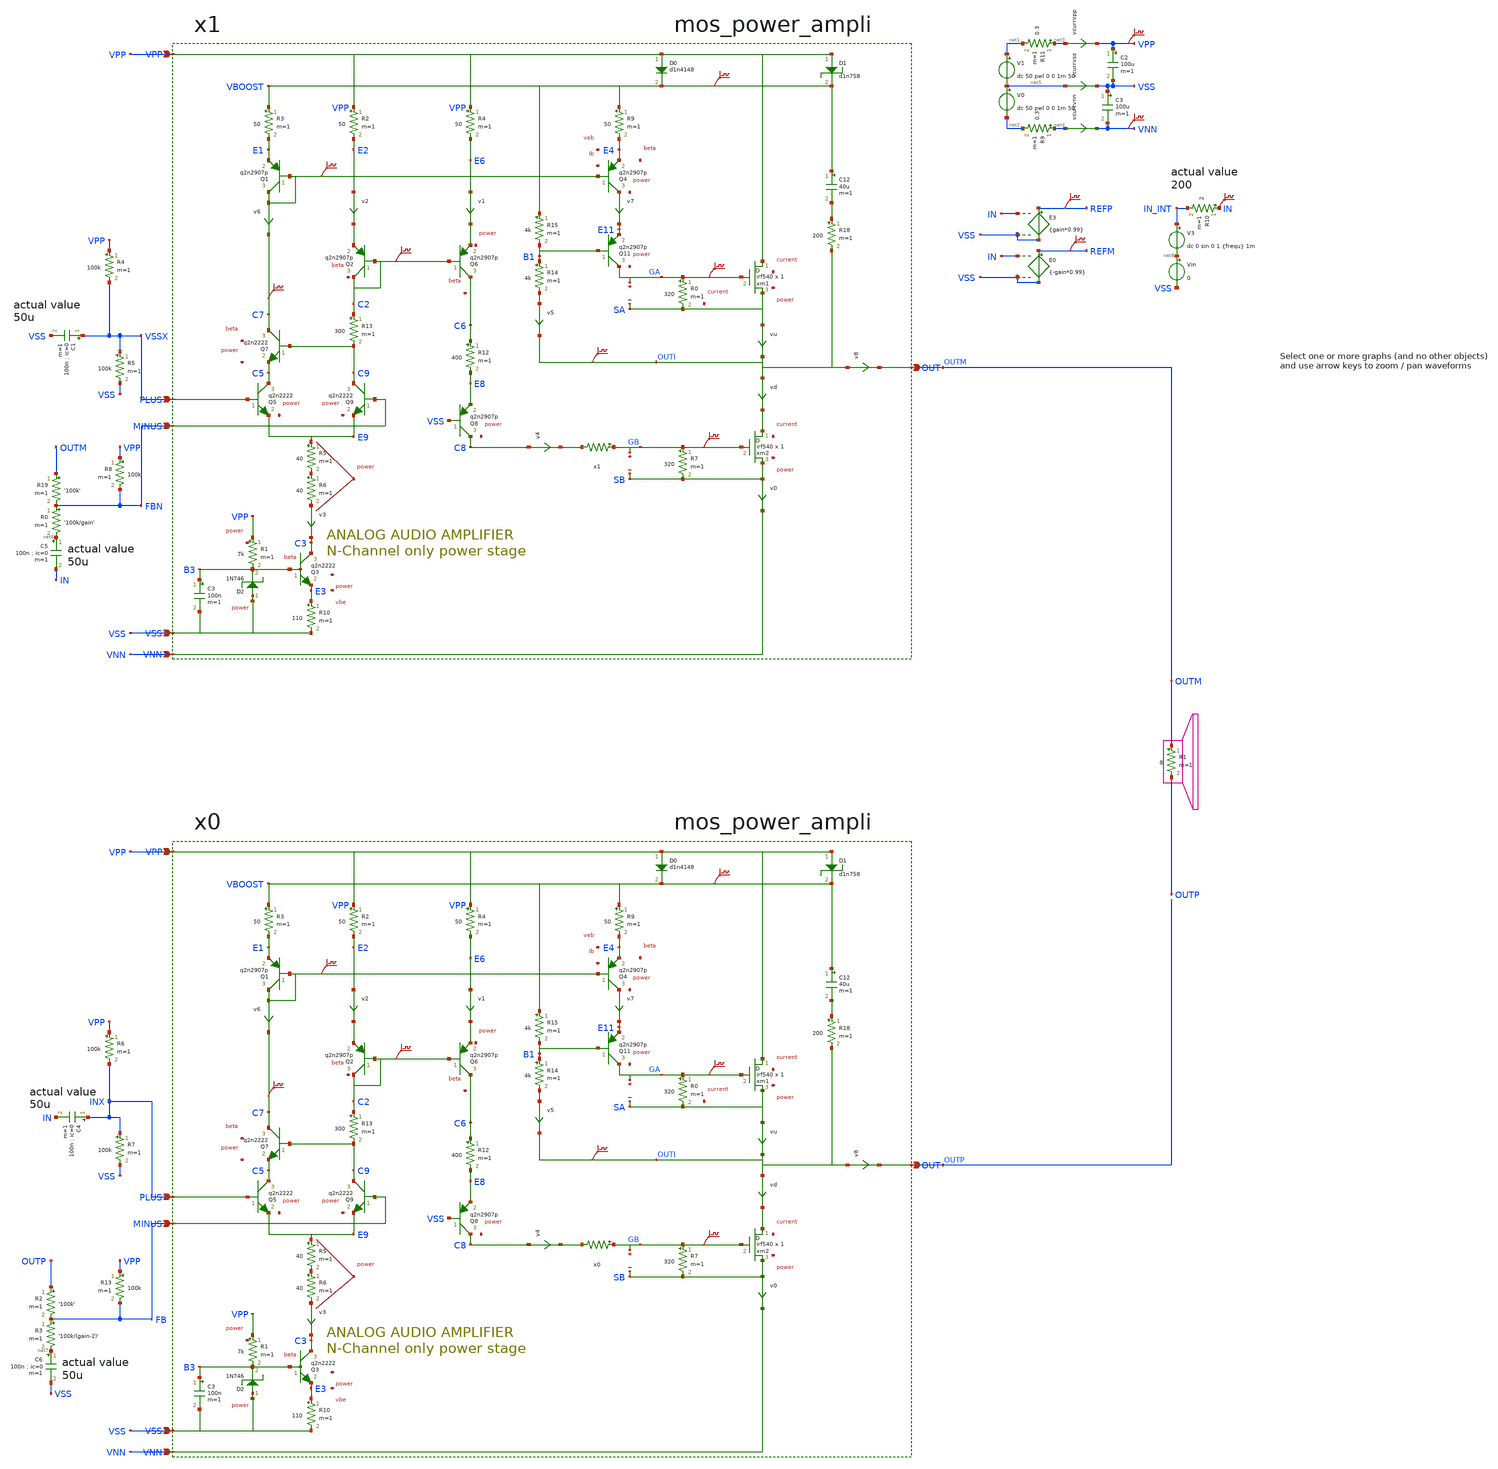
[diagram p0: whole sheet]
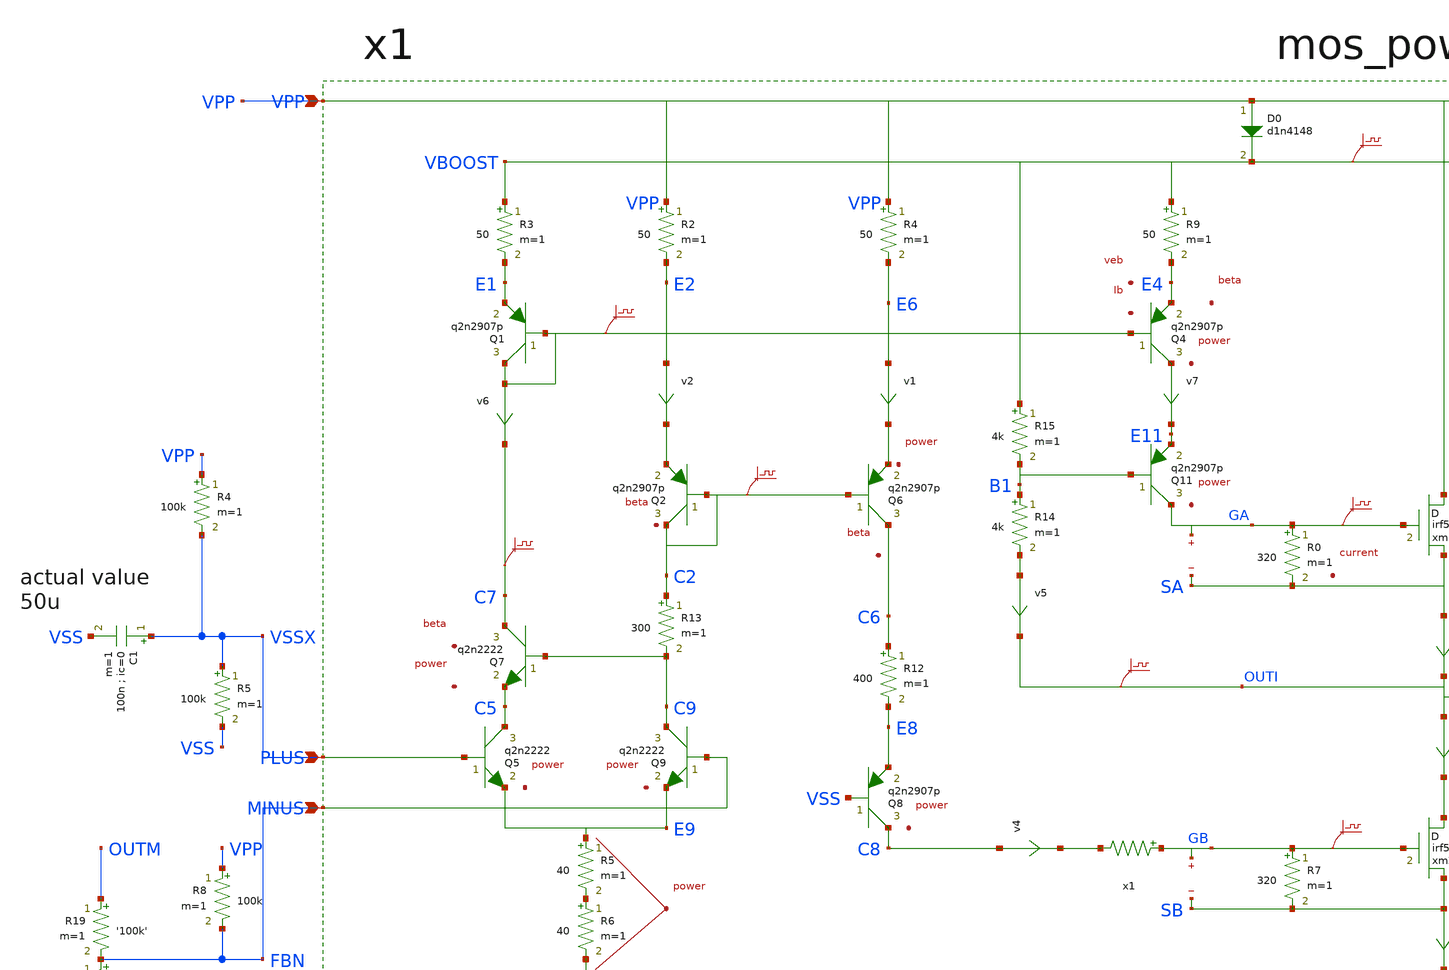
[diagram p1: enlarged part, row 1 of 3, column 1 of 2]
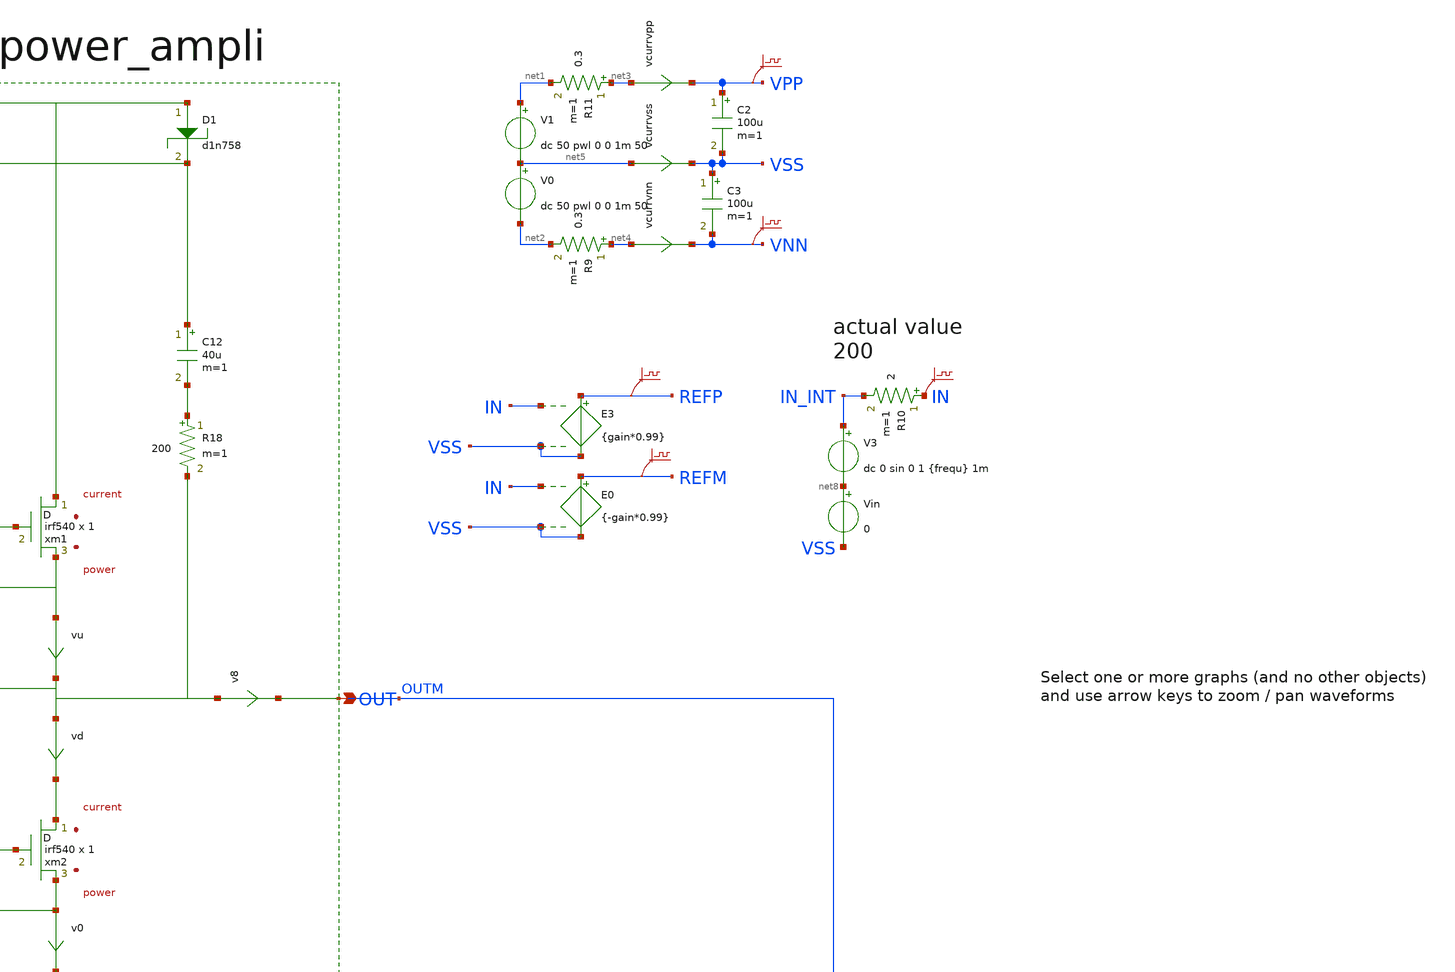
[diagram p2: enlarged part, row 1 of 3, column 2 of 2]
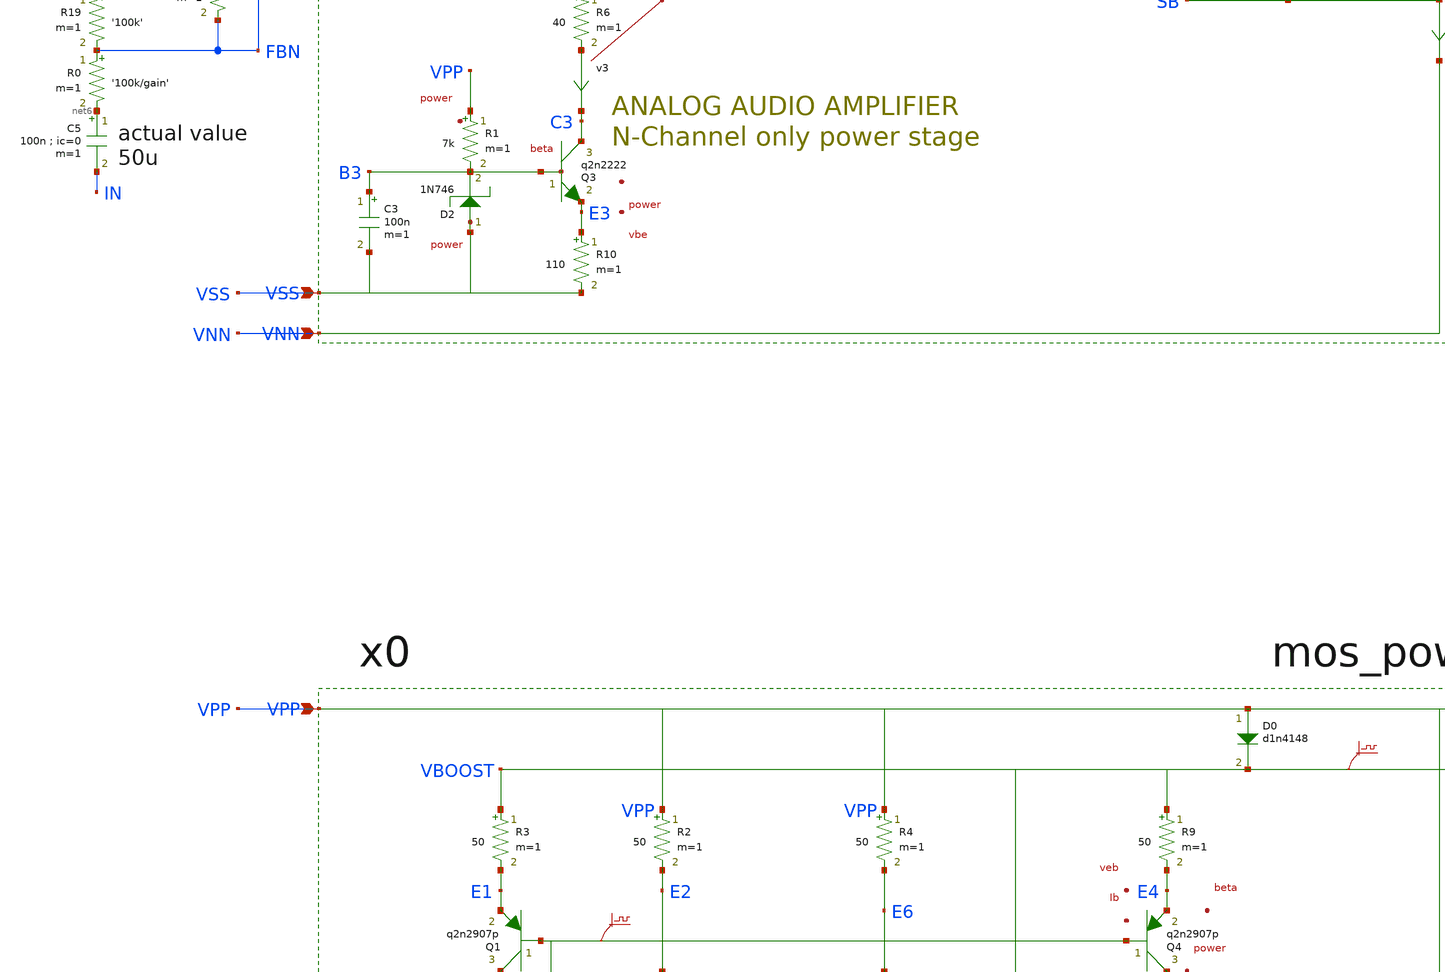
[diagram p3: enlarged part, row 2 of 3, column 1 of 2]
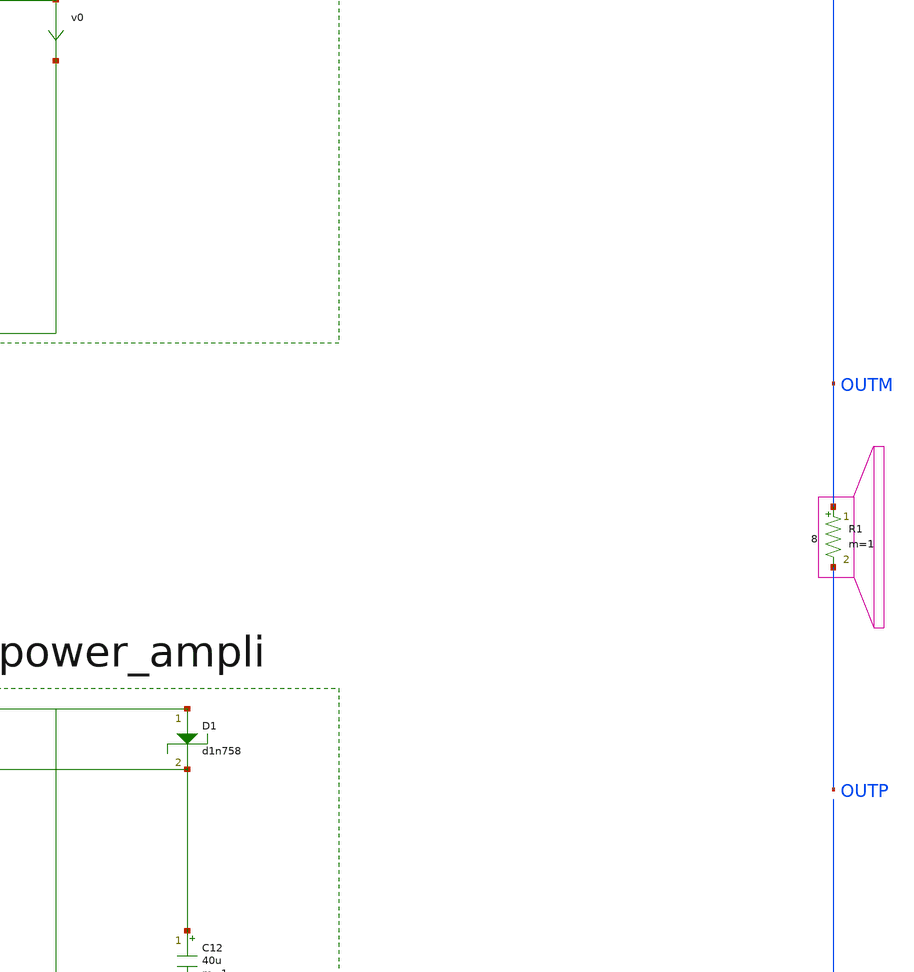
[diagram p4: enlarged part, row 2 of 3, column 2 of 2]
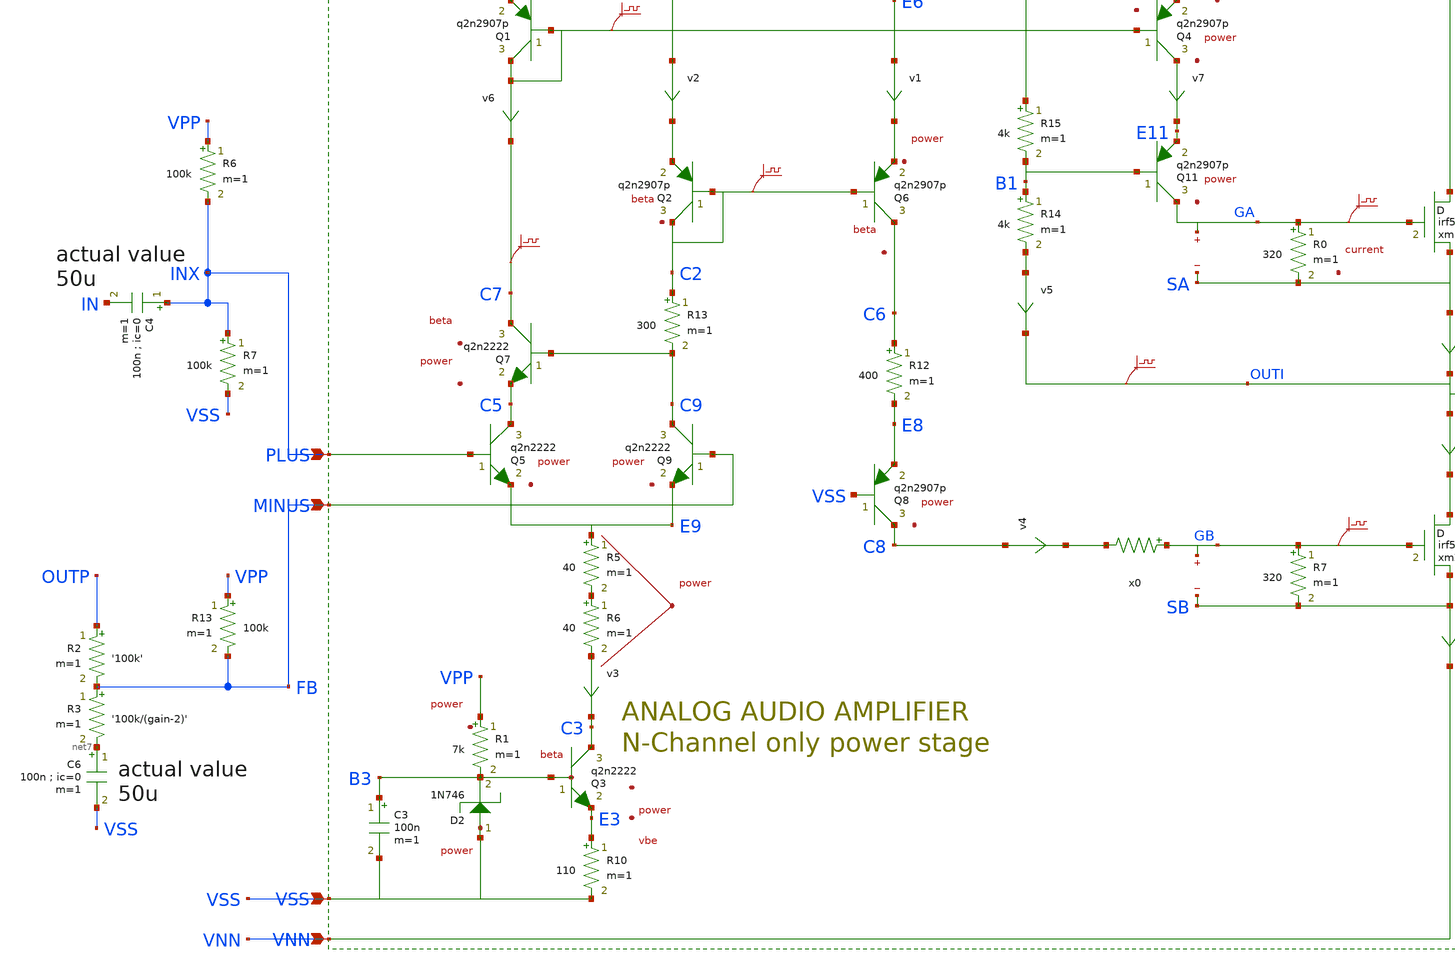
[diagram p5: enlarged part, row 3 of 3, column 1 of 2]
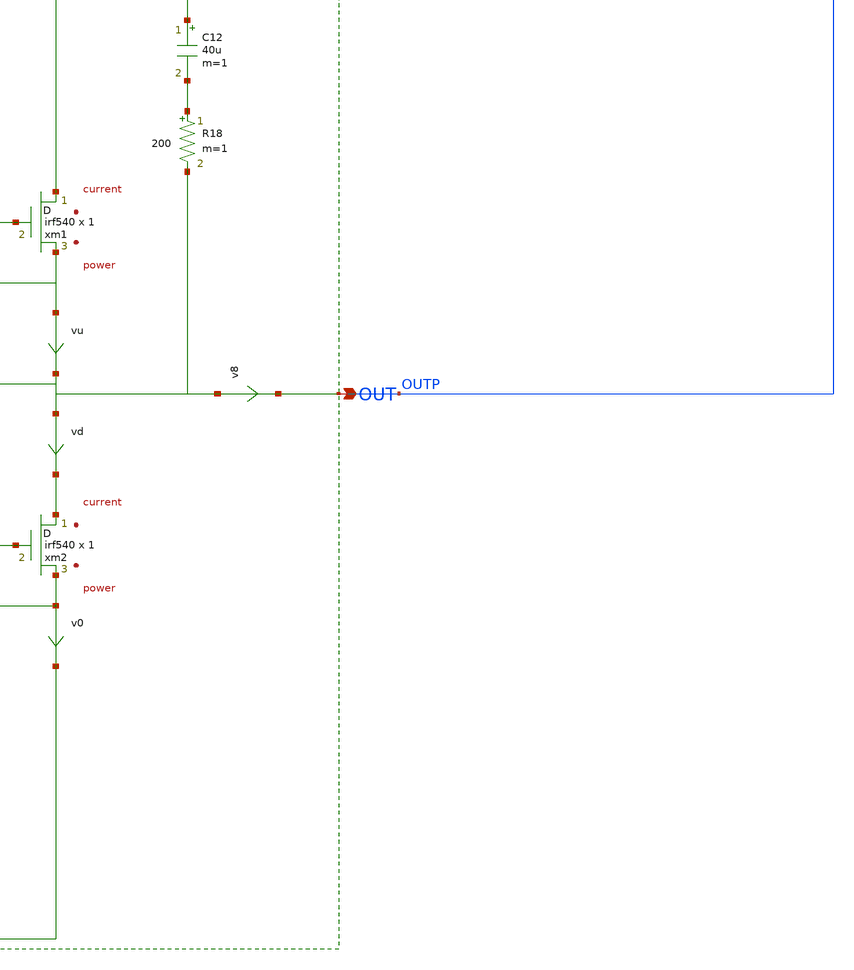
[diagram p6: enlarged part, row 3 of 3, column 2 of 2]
** sch_path: xschem-src/xschem_library/examples/poweramp_lcc.sch
* Copyright (C) 1998-2026 Stefan Frederik Schippers
* This program is free software; you can redistribute it and/or modify
* it under the terms of the GNU General Public License as published by
* the Free Software Foundation; either version 2 of the License, or
* (at your option) any later version.
* This program is distributed in the hope that it will be useful,
* but WITHOUT ANY WARRANTY; without even the implied warranty of
* MERCHANTABILITY or FITNESS FOR A PARTICULAR PURPOSE.  See the
* GNU General Public License for more details.
* You should have received a copy of the GNU General Public License
* along with this program; if not, write to the Free Software
**.subckt poweramp_lcc
V1 net1 net5 dc 50 pwl 0 0 1m 50
V0 net5 net2 dc 50 pwl 0 0 1m 50
R1 OUTM OUTP 8 m=1
E3 REFP VSS IN VSS {gain*0.99}
C3 VSS VNN 100u m=1
R11 net3 net1 0.3 m=1
R9 net4 net2 0.3 m=1
R19 OUTM FBN '100k' m=1
R0 FBN net6 '100k/gain' m=1
R6 VPP INX 100k m=1
R7 INX VSS 100k m=1
E0 REFM VSS IN VSS {-gain*0.99}
C5 net6 IN 100n ; ic=0 m=1
C6 net7 VSS 100n ; ic=0 m=1
R2 OUTP FB '100k' m=1
R3 FB net7 '100k/(gain-2)' m=1
V3 IN_INT net8 dc 0 sin 0 1 {frequ} 1m
R4 VPP VSSX 100k m=1
R5 VSSX VSS 100k m=1
R8 VPP FBN 100k m=1
C4 INX IN 100n ; ic=0 m=1
C1 VSSX VSS 100n ; ic=0 m=1
R10 IN IN_INT 2 m=1
R13 VPP FB 100k m=1
Vin net8 VSS 0
vcurrvpp net3 VPP 0
.save i(vcurrvpp)
vcurrvnn net4 VNN 0
.save i(vcurrvnn)
vcurrvss net5 VSS 0
.save i(vcurrvss)
C2 VPP VSS 100u m=1
.save v(refp)
.save v(refm)
.save v(in)
.save v(vpp)
.save v(vnn)
x0 FB INX VSS OUTP VPP VNN mos_power_ampli
x1 FBN VSSX VSS OUTM VPP VNN mos_power_ampli
**** begin user architecture code



.option ITL4=20000 ITL5=0
vvss vss 0 dc 0
.temp 30

.param frequ=5k
.param gain=45
.option savecurrents

** models are generally not free: you must download
** SPICE models for active devices and put them  into the below
** referenced file in simulation directory.
.include "models_poweramp.txt"
.control
save all
op
write poweramp_lcc.raw
set appendwrite
tran  8e-7 0.02 uic
* .FOUR 20k v(outm,outp)
* .probe i(*)
plot outp outm
save p(r*) p(v*)
write poweramp_lcc.raw
.endc






**** end user architecture code
**.ends

* expanding   symbol:  mos_power_ampli.sch # of pins=6
** sym_path: xschem-src/xschem_library/examples/mos_power_ampli.sch
** sch_path: xschem-src/xschem_library/examples/mos_power_ampli.sch
.subckt mos_power_ampli MINUS PLUS VSS OUT VPP VNN
*.ipin PLUS
*.ipin VNN
*.opin OUT
*.ipin MINUS
*.ipin VSS
*.ipin VPP
xm2 net1 GB SB irf540 m=1
R7 GB SB 320 m=1
xm1 VPP GA SA irf540 m=1
R0 GA SA 320 m=1
R2 VPP E2 50 m=1
R3 VBOOST E1 50 m=1
Q5 C5 PLUS E9 q2n2222 area=1 m=1
Q4 net8 net2 E4 q2n2907p area=1 m=1
R9 VBOOST E4 50 m=1
Q6 C6 C2 net5 q2n2907p area=1 m=1
R4 VPP E6 50 m=1
vd OUTI net1 0
.save i(vd)
vu SA OUTI 0
.save i(vu)
Q1 net2 net2 E1 q2n2907p area=1 m=1
Q2 C2 C2 net4 q2n2907p area=1 m=1
Q9 C9 MINUS E9 q2n2222 area=1 m=1
R11 GB net6 1000 m=1
Q8 C8 VSS E8 q2n2907p area=1 m=1
C12 VBOOST net3 40u m=1
D0 VPP VBOOST d1n4148 area=1
R18 net3 OUTI 200 m=1
D1 VPP VBOOST d1n758
R14 B1 net7 4k m=1
Q11 GA B1 E11 q2n2907p area=1 m=1
R15 VBOOST B1 4k m=1
R5 E9 net9 40 m=1
R6 net9 net10 40 m=1
D2 VSS B3 1N746
Q3 C3 B3 E3 q2n2222 area=1 m=1
R1 VPP B3 7k m=1
R10 E3 VSS 110 m=1
C3 B3 VSS 100n m=1
R12 C6 E8 400 m=1
R13 C2 C9 300 m=1
Q7 C7 C9 C5 q2n2222 area=1 m=1
v0 SB VNN 0
.save i(v0)
v1 E6 net5 0
.save i(v1)
v2 E2 net4 0
.save i(v2)
v3 net10 C3 0
.save i(v3)
v4 C8 net6 0
.save i(v4)
v5 net7 OUTI 0
.save i(v5)
v6 net2 C7 0
.save i(v6)
v7 net8 E11 0
.save i(v7)
.save v(gb)
.save v(sb)
.save v(ga)
.save v(sa)
v8 OUTI OUT 0
.save i(v8)
.save v(ga)
.save v(gb)
.save v(c2)
.save v(net2)
.save v(c7)
.save v(vboost)
.save v(outi)
.ends

.end
